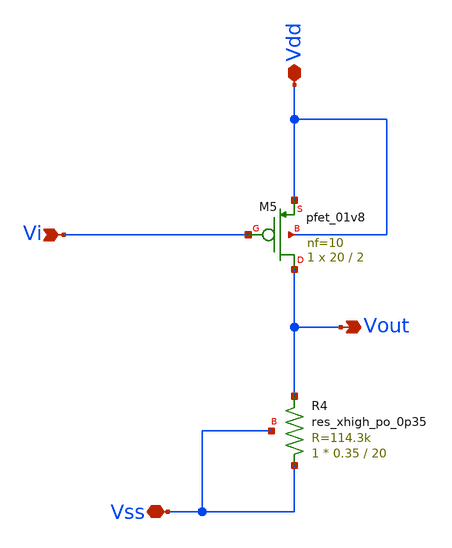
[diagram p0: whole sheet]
** sch_path: Circuits/DiffAmp/CMS_Amp.sch
**.subckt CMS_Amp Vout Vi Vdd Vss
*.opin Vout
*.ipin Vi
*.iopin Vdd
*.iopin Vss
XM5 Vout Vi Vdd Vdd sky130_fd_pr__pfet_01v8 L=2 W=20 nf=10 ad='int((nf+1)/2) * W/nf * 0.29' as='int((nf+2)/2) * W/nf * 0.29'
+ pd='2*int((nf+1)/2) * (W/nf + 0.29)' ps='2*int((nf+2)/2) * (W/nf + 0.29)' nrd='0.29 / W' nrs='0.29 / W'
+ sa=0 sb=0 sd=0 mult=1 m=1
XR4 Vss Vout Vss sky130_fd_pr__res_xhigh_po_0p35 L=20 mult=1 m=1
**.ends
.end
